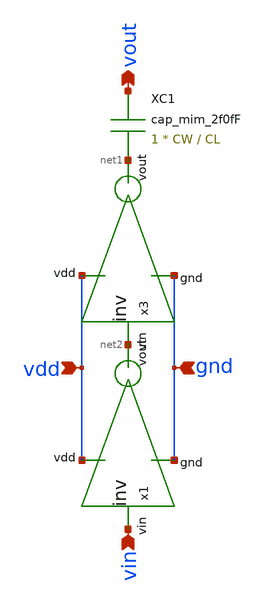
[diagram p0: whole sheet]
** sch_path: SAR_ADC/xschem/designs/cdac_line.sch
**.subckt cdac_line vdd gnd vin vout
*.ipin vdd
*.ipin gnd
*.ipin vin
*.opin vout
XC1 vout net1 cap_mim_2f0fF c_width=CW c_length=CL m=1
x3 vdd gnd net1 net2 inv cl=0.28u wp=0.44u wn=0.22u wx=0.22u
x1 vdd gnd net2 vin inv cl=0.28u wp=0.44u wn=0.22u wx=0.22u
**.ends

* expanding   symbol:  inv.sym # of pins=4
** sym_path: SAR_ADC/xschem/designs/inv.sym
** sch_path: SAR_ADC/xschem/designs/inv.sch
.subckt inv vdd gnd vout vin  cl=0.28u wp=0.44u wn=0.22u wx=0.22u
*.ipin gnd
*.ipin vdd
*.ipin vin
*.opin vout
XM1 gnd vin vout gnd nfet_03v3 L=0.28u W=8u nf=1 ad='int((nf+1)/2) * W/nf * 0.18u' as='int((nf+2)/2) * W/nf * 0.18u'
+ pd='2*int((nf+1)/2) * (W/nf + 0.18u)' ps='2*int((nf+2)/2) * (W/nf + 0.18u)' nrd='0.18u / W' nrs='0.18u / W'
+ sa=0 sb=0 sd=0 m=1
XM2 vdd vin vout vdd pfet_03v3 L=0.28u W=8u nf=1 ad='int((nf+1)/2) * W/nf * 0.18u' as='int((nf+2)/2) * W/nf * 0.18u'
+ pd='2*int((nf+1)/2) * (W/nf + 0.18u)' ps='2*int((nf+2)/2) * (W/nf + 0.18u)' nrd='0.18u / W' nrs='0.18u / W'
+ sa=0 sb=0 sd=0 m=1
.ends

.end
